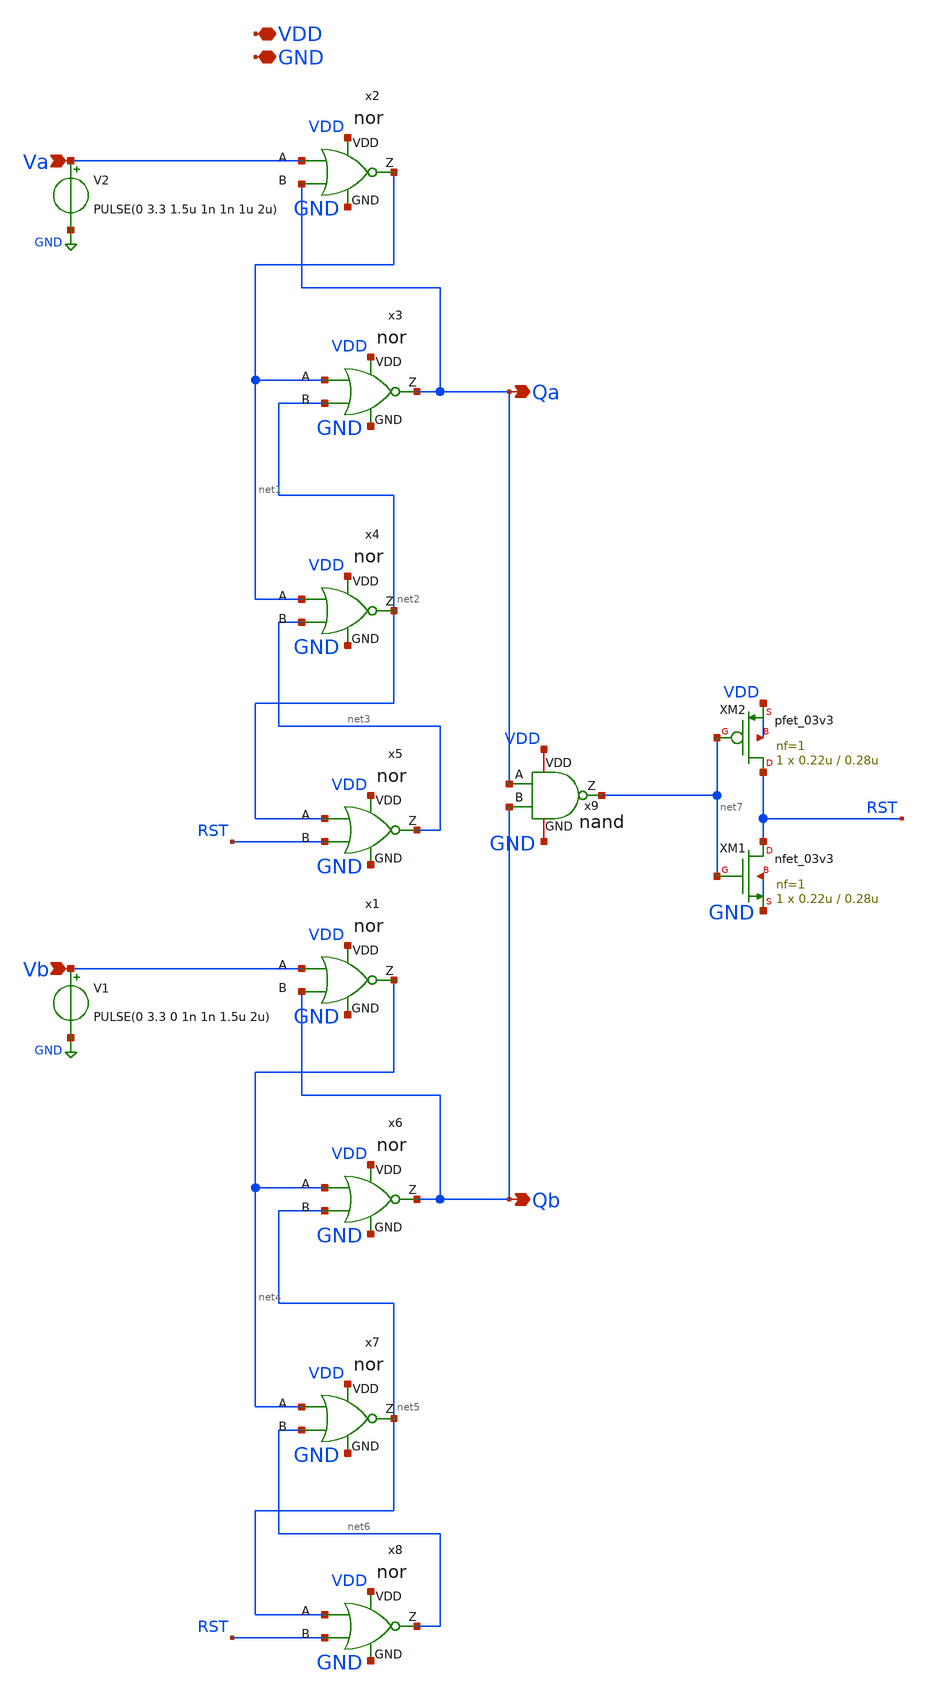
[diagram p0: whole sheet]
** sch_path: pll_block_templates_v1/layout2/pfd.sch
**.subckt pfd Vb Va Qa Qb VDD GND
*.ipin Vb
*.ipin Va
*.opin Qa
*.opin Qb
*.iopin VDD
*.iopin GND
x2 VDD Va Qa net1 GND nor
x3 VDD net1 net2 Qa GND nor
x4 VDD net1 net3 net2 GND nor
V2 Va GND PULSE(0 3.3 1.5u 1n 1n 1u 2u)
x5 VDD net2 RST net3 GND nor
x1 VDD Vb Qb net4 GND nor
x6 VDD net4 net5 Qb GND nor
x7 VDD net4 net6 net5 GND nor
V1 Vb GND PULSE(0 3.3 0 1n 1n 1.5u 2u)
x8 VDD net5 RST net6 GND nor
x9 VDD net7 Qa Qb GND nand
XM1 RST net7 GND GND nfet_03v3 L=0.28u W=0.22u nf=1 ad='int((nf+1)/2) * W/nf * 0.18u' as='int((nf+2)/2) * W/nf * 0.18u'
+ pd='2*int((nf+1)/2) * (W/nf + 0.18u)' ps='2*int((nf+2)/2) * (W/nf + 0.18u)' nrd='0.18u / W' nrs='0.18u / W'
+ sa=0 sb=0 sd=0 m=1
XM2 RST net7 VDD VDD pfet_03v3 L=0.28u W=0.22u nf=1 ad='int((nf+1)/2) * W/nf * 0.18u' as='int((nf+2)/2) * W/nf * 0.18u'
+ pd='2*int((nf+1)/2) * (W/nf + 0.18u)' ps='2*int((nf+2)/2) * (W/nf + 0.18u)' nrd='0.18u / W' nrs='0.18u / W'
+ sa=0 sb=0 sd=0 m=1
**** begin user architecture code

.include $::180MCU_MODELS/design.ngspice
.lib $::180MCU_MODELS/sm141064.ngspice typical
.lib $::180MCU_MODELS/sm141064.ngspice res_typical
.lib $::180MCU_MODELS/sm141064.ngspice moscap_typical
* .lib $::180MCU_MODELS/sm141064.ngspice res_statistical
.lib $::180MCU_MODELS/sm141064.ngspice cap_mim
.lib $::180MCU_MODELS/sm141064.ngspice mimcap_typical



V_VDD vdd 0 3.3v
* V_RST rst 0 pulse(0 3.3 0 1n 1n 10u 20u)
.control
save all
tran 0.10u 30u
plot v(qa) v(qb)
plot v(net1) v(net5)
write VCO_GF180.raw
.endc


**** end user architecture code
**.ends

* expanding   symbol:  blocks/pll/nor.sym # of pins=5
** sym_path: blocks/pll/nor.sym
** sch_path: blocks/pll/nor.sch
.subckt nor VDD A B Z GND
*.ipin A
*.ipin B
*.opin Z
*.iopin GND
*.iopin VDD
XM1 Z A GND GND nfet_03v3 L=0.28u W=0.22u nf=1 ad='int((nf+1)/2) * W/nf * 0.18u' as='int((nf+2)/2) * W/nf * 0.18u'
+ pd='2*int((nf+1)/2) * (W/nf + 0.18u)' ps='2*int((nf+2)/2) * (W/nf + 0.18u)' nrd='0.18u / W' nrs='0.18u / W'
+ sa=0 sb=0 sd=0 m=1
XM2 Z B net1 VDD pfet_03v3 L=0.28u W=0.22u nf=1 ad='int((nf+1)/2) * W/nf * 0.18u' as='int((nf+2)/2) * W/nf * 0.18u'
+ pd='2*int((nf+1)/2) * (W/nf + 0.18u)' ps='2*int((nf+2)/2) * (W/nf + 0.18u)' nrd='0.18u / W' nrs='0.18u / W'
+ sa=0 sb=0 sd=0 m=1
XM3 Z B GND GND nfet_03v3 L=0.28u W=0.22u nf=1 ad='int((nf+1)/2) * W/nf * 0.18u' as='int((nf+2)/2) * W/nf * 0.18u'
+ pd='2*int((nf+1)/2) * (W/nf + 0.18u)' ps='2*int((nf+2)/2) * (W/nf + 0.18u)' nrd='0.18u / W' nrs='0.18u / W'
+ sa=0 sb=0 sd=0 m=1
XM4 net1 A VDD VDD pfet_03v3 L=0.28u W=0.22u nf=1 ad='int((nf+1)/2) * W/nf * 0.18u' as='int((nf+2)/2) * W/nf * 0.18u'
+ pd='2*int((nf+1)/2) * (W/nf + 0.18u)' ps='2*int((nf+2)/2) * (W/nf + 0.18u)' nrd='0.18u / W' nrs='0.18u / W'
+ sa=0 sb=0 sd=0 m=1
.ends


* expanding   symbol:  blocks/pll/nand.sym # of pins=5
** sym_path: pll_block_templates_v1/layout2/nand.sym
** sch_path: pll_block_templates_v1/layout2/nand.sch
.subckt nand VDD Z A B GND
*.ipin A
*.iopin VDD
*.opin Z
*.iopin GND
*.ipin B
XM1 Z A net1 GND nfet_03v3 L=0.28u W=0.3u nf=1 ad='int((nf+1)/2) * W/nf * 0.18u' as='int((nf+2)/2) * W/nf * 0.18u'
+ pd='2*int((nf+1)/2) * (W/nf + 0.18u)' ps='2*int((nf+2)/2) * (W/nf + 0.18u)' nrd='0.18u / W' nrs='0.18u / W'
+ sa=0 sb=0 sd=0 m=1
XM2 Z A VDD VDD pfet_03v3 L=0.28u W=0.3u nf=1 ad='int((nf+1)/2) * W/nf * 0.18u' as='int((nf+2)/2) * W/nf * 0.18u'
+ pd='2*int((nf+1)/2) * (W/nf + 0.18u)' ps='2*int((nf+2)/2) * (W/nf + 0.18u)' nrd='0.18u / W' nrs='0.18u / W'
+ sa=0 sb=0 sd=0 m=1
XM3 Z B VDD VDD pfet_03v3 L=0.28u W=0.3u nf=1 ad='int((nf+1)/2) * W/nf * 0.18u' as='int((nf+2)/2) * W/nf * 0.18u'
+ pd='2*int((nf+1)/2) * (W/nf + 0.18u)' ps='2*int((nf+2)/2) * (W/nf + 0.18u)' nrd='0.18u / W' nrs='0.18u / W'
+ sa=0 sb=0 sd=0 m=1
XM4 net1 B GND GND nfet_03v3 L=0.28u W=0.3u nf=1 ad='int((nf+1)/2) * W/nf * 0.18u' as='int((nf+2)/2) * W/nf * 0.18u'
+ pd='2*int((nf+1)/2) * (W/nf + 0.18u)' ps='2*int((nf+2)/2) * (W/nf + 0.18u)' nrd='0.18u / W' nrs='0.18u / W'
+ sa=0 sb=0 sd=0 m=1
.ends

.GLOBAL GND
.end
